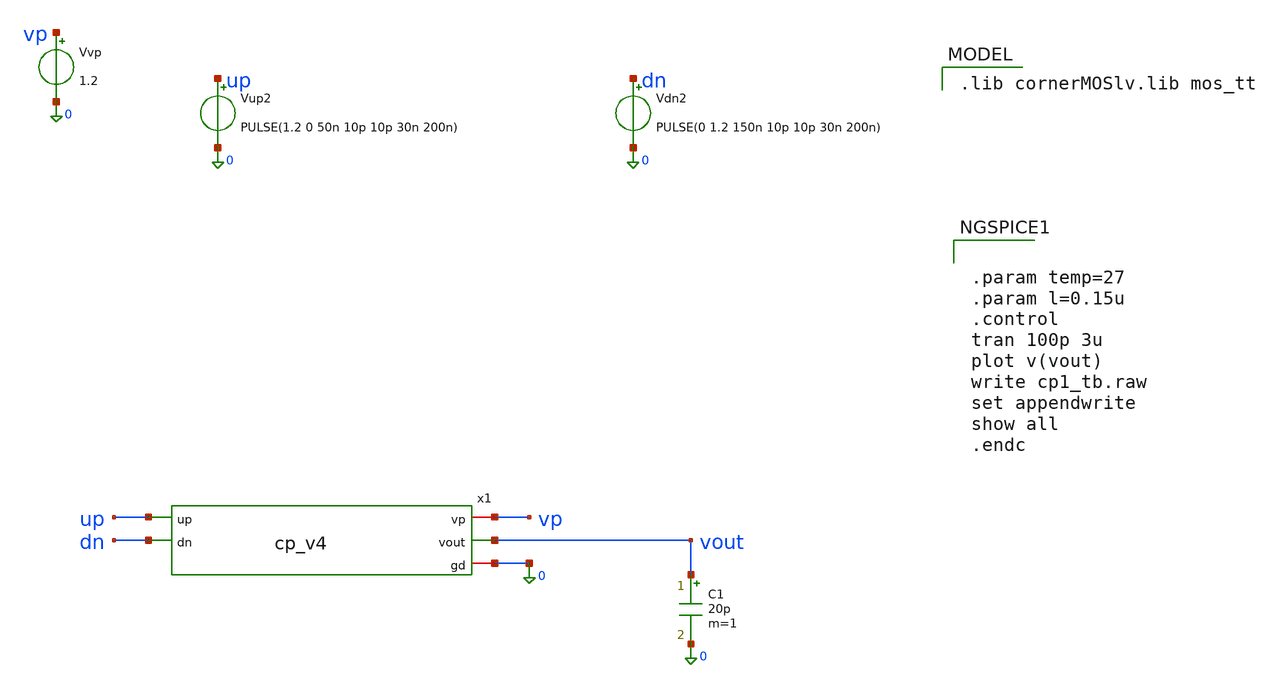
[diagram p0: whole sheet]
** sch_path: schematics/charge_pump/old_sch/cp_v4_tb.sch
**.subckt cp_v4_tb
Vvp vp 0 1.2
C1 vout 0 20p m=1
x1 vp up vout dn 0 cp_v4
Vup2 up 0 PULSE(1.2 0 50n 10p 10p 30n 200n)
Vdn2 dn 0 PULSE(0 1.2 150n 10p 10p 30n 200n)
**** begin user architecture code
 .lib cornerMOSlv.lib mos_tt



.param temp=27
.param l=0.15u
.control
tran 100p 3u
plot v(vout)
write cp1_tb.raw
set appendwrite
show all
.endc


**** end user architecture code
**.ends
.end
